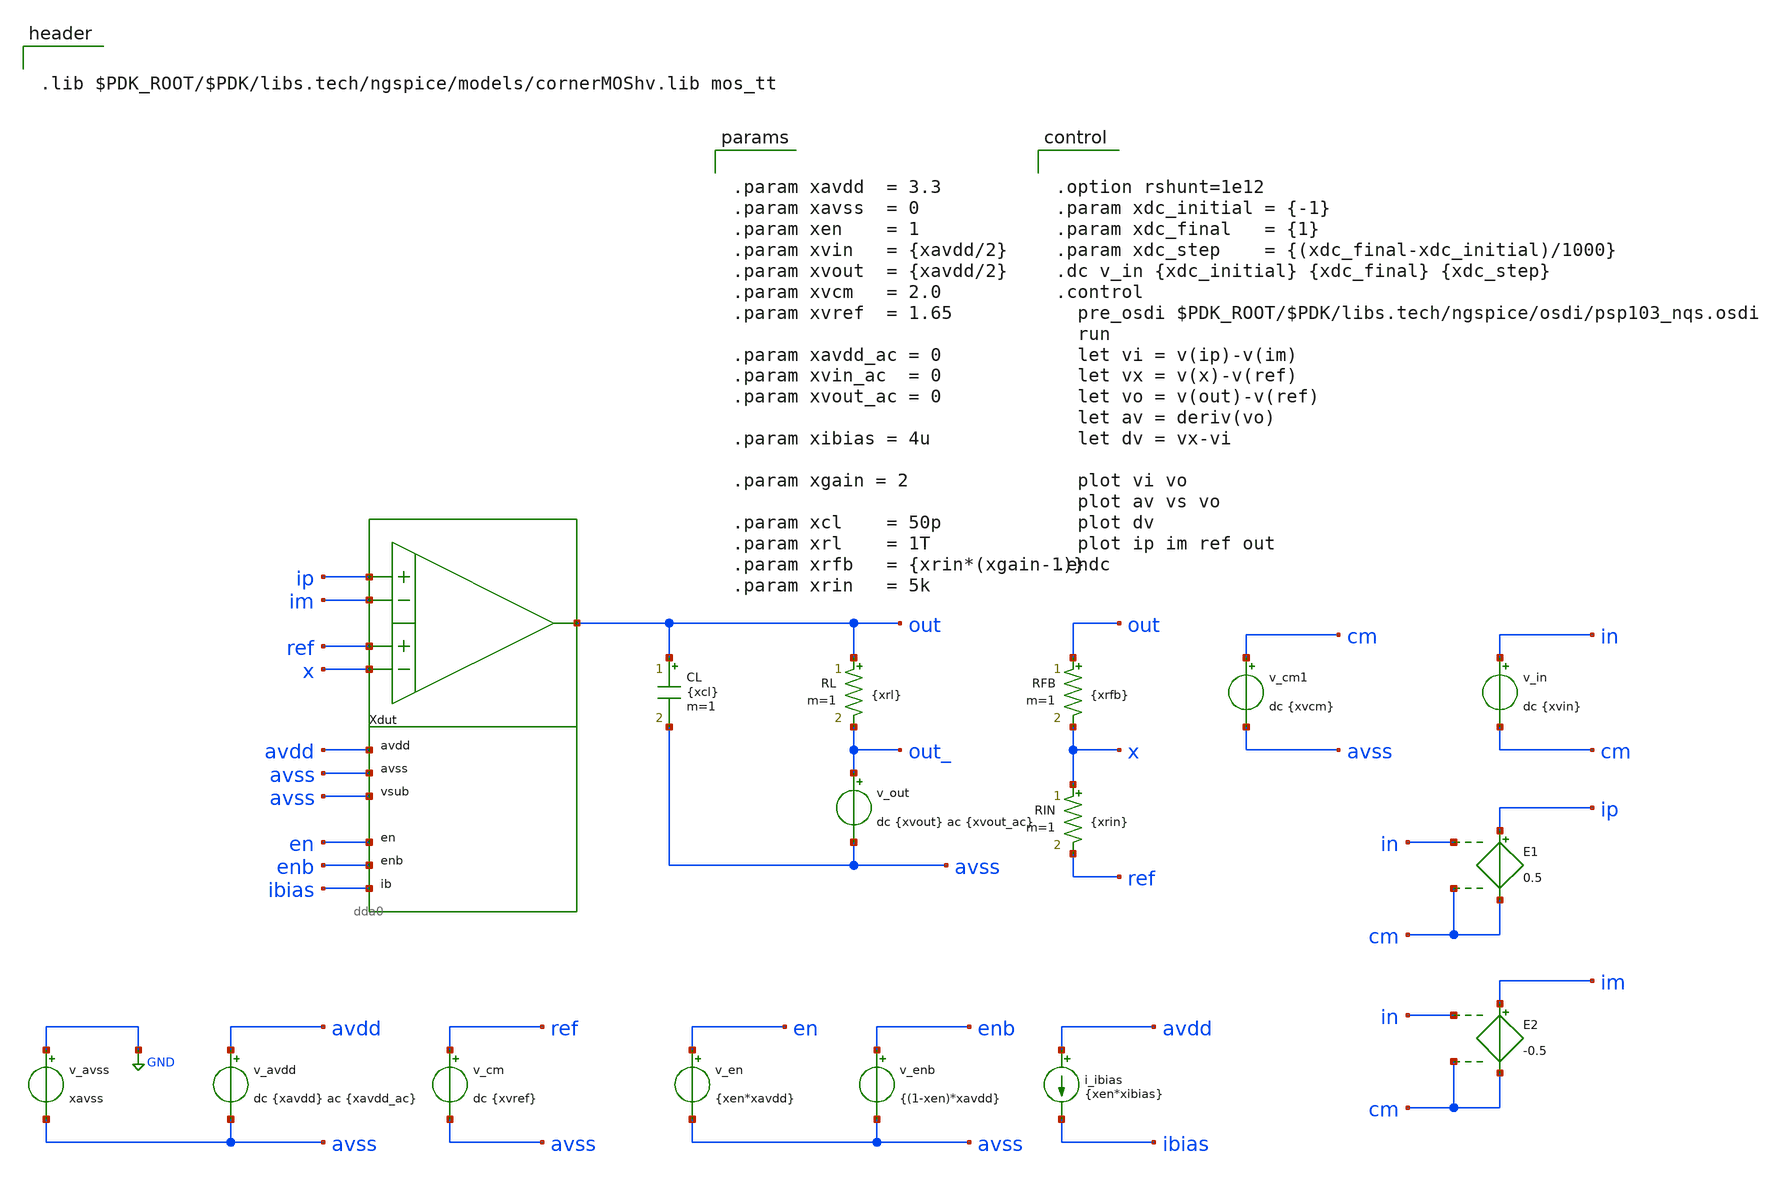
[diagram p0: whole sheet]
** sch_path: xschem/tb_dda0_amp_dc.sch
**.subckt tb_dda0_amp_dc
Xdut ip im ref x out avdd avss avss en enb ibias dda0
v_avss GND avss xavss
v_avdd avdd avss dc {xavdd} ac {xavdd_ac}
v_en en avss {xen*xavdd}
v_enb enb avss {(1-xen)*xavdd}
i_ibias avdd ibias {xen*xibias}
CL out avss {xcl} m=1
v_out out_ avss dc {xvout} ac {xvout_ac}
RL out out_ {xrl} m=1
RFB out x {xrfb} m=1
RIN x ref {xrin} m=1
v_cm ref avss dc {xvref}
v_cm1 cm avss dc {xvcm}
v_in in cm dc {xvin}
E1 ip cm in cm 0.5
E2 im cm in cm -0.5
**** begin user architecture code


.lib $PDK_ROOT/$PDK/libs.tech/ngspice/models/cornerMOShv.lib mos_tt




.option rshunt=1e12
.param xdc_initial = {-1}
.param xdc_final   = {1}
.param xdc_step    = {(xdc_final-xdc_initial)/1000}
.dc v_in {xdc_initial} {xdc_final} {xdc_step}
.control
  pre_osdi $PDK_ROOT/$PDK/libs.tech/ngspice/osdi/psp103_nqs.osdi
  run
  let vi = v(ip)-v(im)
  let vx = v(x)-v(ref)
  let vo = v(out)-v(ref)
  let av = deriv(vo)
  let dv = vx-vi

  plot vi vo
  plot av vs vo
  plot dv
  plot ip im ref out
.endc




.param xavdd  = 3.3
.param xavss  = 0
.param xen    = 1
.param xvin   = {xavdd/2}
.param xvout  = {xavdd/2}
.param xvcm   = 2.0
.param xvref  = 1.65

.param xavdd_ac = 0
.param xvin_ac  = 0
.param xvout_ac = 0

.param xibias = 4u

.param xgain = 2

.param xcl    = 50p
.param xrl    = 1T
.param xrfb   = {xrin*(xgain-1)}
.param xrin   = 5k


**** end user architecture code
**.ends
.GLOBAL GND
.end
